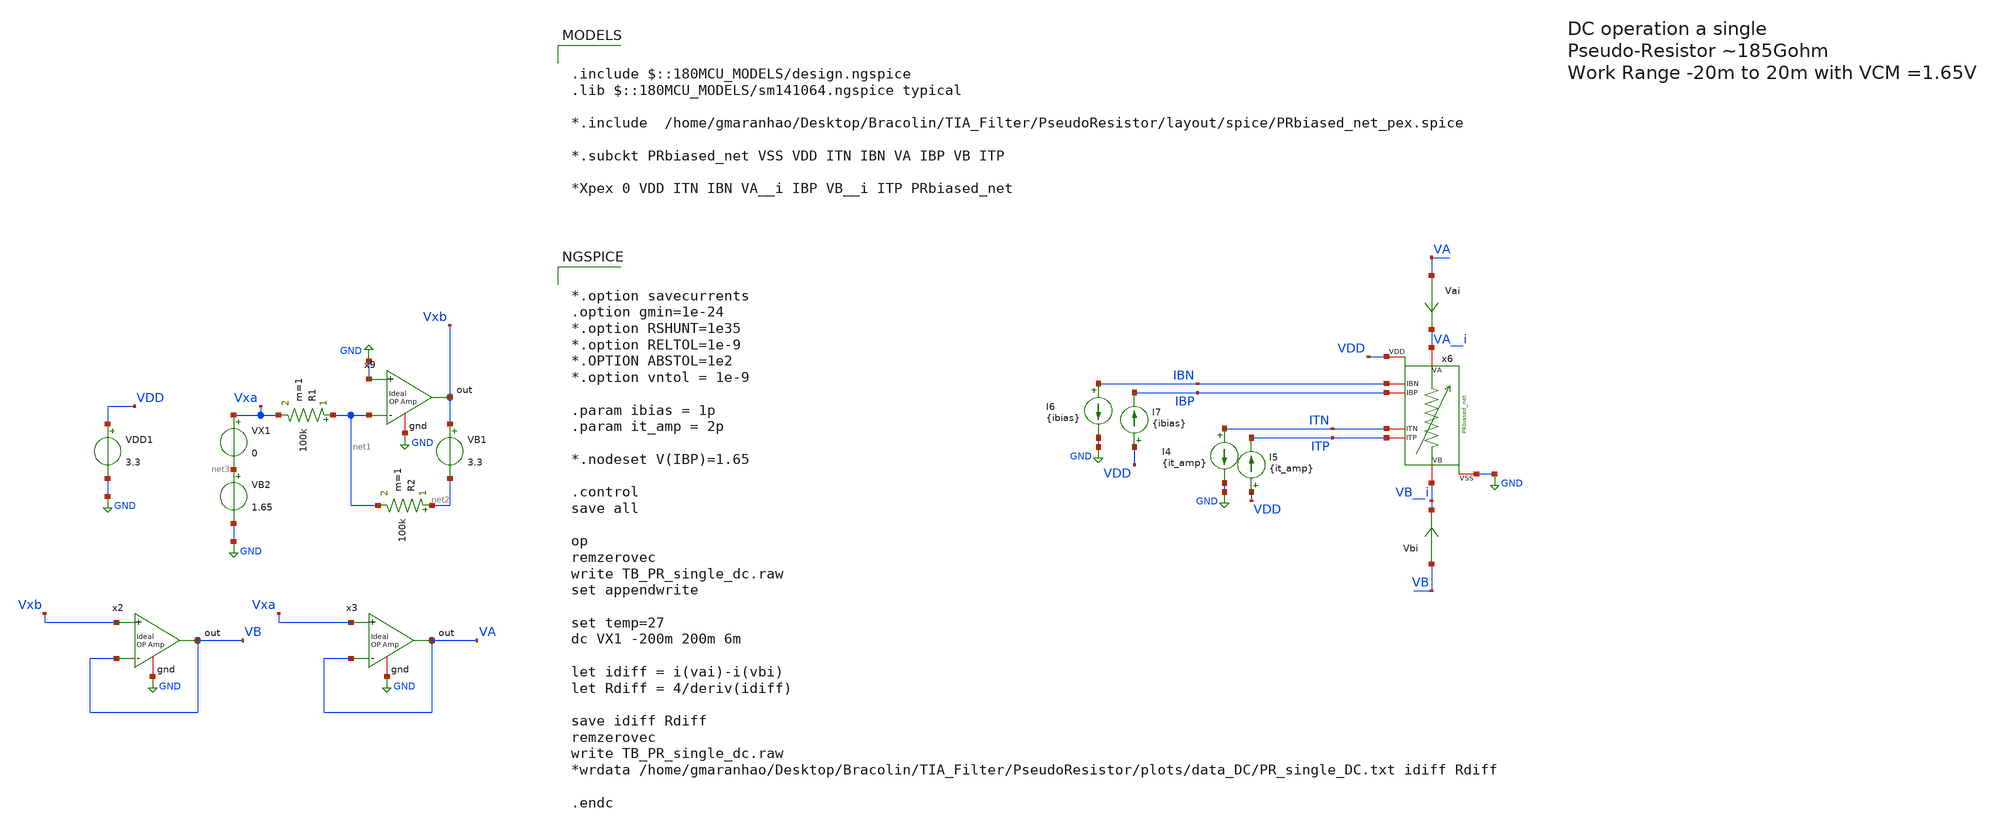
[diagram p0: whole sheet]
** sch_path: TIA_Filter/PseudoResistor/TB_PR_single_dc.sch
**.subckt TB_PR_single_dc
x6 VA__i VB__i IBN IBP ITN ITP VDD GND PRbiased_net
I4 ITN GND {it_amp}
I5 VDD ITP {it_amp}
I6 IBN GND {ibias}
I7 VDD IBP {ibias}
Vai VA VA__i 0
.save i(vai)
Vbi VB VB__i 0
.save i(vbi)
VDD1 VDD GND 3.3
VX1 Vxa net3 0
VB1 Vxb net2 3.3
R1 net1 Vxa 100k m=1
R2 net2 net1 100k m=1
VB2 net3 GND 1.65
x2 VB Vxb VB GND ampOp_ideal
x3 VA Vxa VA GND ampOp_ideal
x9 Vxb GND net1 GND ampOp_ideal
**** begin user architecture code

.include $::180MCU_MODELS/design.ngspice
.lib $::180MCU_MODELS/sm141064.ngspice typical

*.include  /home/gmaranhao/Desktop/Bracolin/TIA_Filter/PseudoResistor/layout/spice/PRbiased_net_pex.spice

*.subckt PRbiased_net VSS VDD ITN IBN VA IBP VB ITP

*Xpex 0 VDD ITN IBN VA__i IBP VB__i ITP PRbiased_net




*.option savecurrents
.option gmin=1e-24
*.option RSHUNT=1e35
*.option RELTOL=1e-9
*.OPTION ABSTOL=1e2
*.option vntol = 1e-9

.param ibias = 1p
.param it_amp = 2p

*.nodeset V(IBP)=1.65

.control
save all

op
remzerovec
write TB_PR_single_dc.raw
set appendwrite

set temp=27
dc VX1 -200m 200m 6m

let idiff = i(vai)-i(vbi)
let Rdiff = 4/deriv(idiff)

save idiff Rdiff
remzerovec
write TB_PR_single_dc.raw
*wrdata /home/gmaranhao/Desktop/Bracolin/TIA_Filter/PseudoResistor/plots/data_DC/PR_single_DC.txt
*+ idiff Rdiff

.endc


**** end user architecture code
**.ends
.GLOBAL GND
.end
